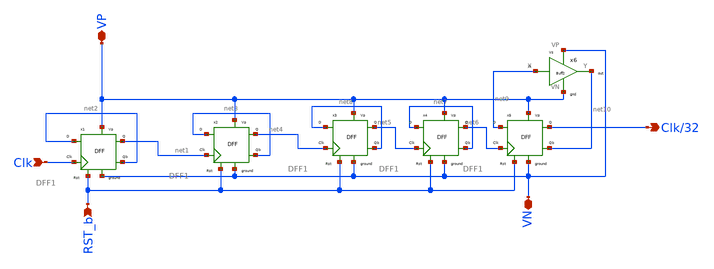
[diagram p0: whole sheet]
** sch_path: Blocks/Divide by 32 ckt/div32.sch
**.subckt div32 Clk/32 Clk VP VN RST_b
*.opin Clk/32
*.ipin Clk
*.iopin VP
*.iopin VN
*.ipin RST_b
x1 net2 Clk RST_b VN VP net1 net2 DFF1
x6 net9 net10 VN VP Buff
x2 net3 net1 RST_b VN VP net4 net3 DFF1
x3 net8 net4 RST_b VN VP net5 net8 DFF1
x4 net7 net5 RST_b VN VP net6 net7 DFF1
x5 net9 net6 RST_b VN VP Clk/32 net10 DFF1
**.ends

* expanding   symbol:  component/FlipFlops/DFF1.sym # of pins=7
** sym_path: component/FlipFlops/DFF1.sym
** sch_path: component/FlipFlops/DFF1.sch
.subckt DFF1 D Clk RST VN VP Q Qb
*.opin Q
*.iopin VN
*.iopin VP
*.ipin Clk
*.ipin D
*.ipin RST
*.opin Qb
x7 net2 net4 net3 VP VN NAND
x8 net3 Clk RST VP VN net2 NAND3
x6 Q net1 RST VP VN Qb NAND3
x4 net2 Clk net4 VP VN net1 NAND3
x5 net1 D RST VP VN net4 NAND3
x1 Qb net2 Q VP VN NAND
.ends


* expanding   symbol:  Blocks/Buffer/Buff.sym # of pins=4
** sym_path: Blocks/Buffer/Buff.sym
** sch_path: Blocks/Buffer/Buff.sch
.subckt Buff X Y VP VN
*.ipin X
*.opin Y
*.iopin VN
*.iopin VP
x1 X net1 VP VN INV
x2 net1 Y VP VN INV
.ends


* expanding   symbol:  component/NAND2/NAND.sym # of pins=5
** sym_path: component/NAND2/NAND.sym
** sch_path: component/NAND2/NAND.sch
.subckt NAND B A Y VP VN
*.iopin VP
*.ipin A
*.ipin B
*.opin Y
*.iopin VN
XM1 Y A VP VP sky130_fd_pr__pfet_01v8 L=0.15 W=1.26 nf=1 ad='int((nf+1)/2) * W/nf * 0.29' as='int((nf+2)/2) * W/nf * 0.29'
+ pd='2*int((nf+1)/2) * (W/nf + 0.29)' ps='2*int((nf+2)/2) * (W/nf + 0.29)' nrd='0.29 / W' nrs='0.29 / W'
+ sa=0 sb=0 sd=0 mult=1 m=1
XM2 Y B VP VP sky130_fd_pr__pfet_01v8 L=0.15 W=1.26 nf=1 ad='int((nf+1)/2) * W/nf * 0.29' as='int((nf+2)/2) * W/nf * 0.29'
+ pd='2*int((nf+1)/2) * (W/nf + 0.29)' ps='2*int((nf+2)/2) * (W/nf + 0.29)' nrd='0.29 / W' nrs='0.29 / W'
+ sa=0 sb=0 sd=0 mult=1 m=1
XM3 Y A net1 net1 sky130_fd_pr__nfet_01v8 L=0.15 W=0.84 nf=1 ad='int((nf+1)/2) * W/nf * 0.29' as='int((nf+2)/2) * W/nf * 0.29'
+ pd='2*int((nf+1)/2) * (W/nf + 0.29)' ps='2*int((nf+2)/2) * (W/nf + 0.29)' nrd='0.29 / W' nrs='0.29 / W'
+ sa=0 sb=0 sd=0 mult=1 m=1
XM4 net1 B VN VN sky130_fd_pr__nfet_01v8 L=0.15 W=0.84 nf=1 ad='int((nf+1)/2) * W/nf * 0.29' as='int((nf+2)/2) * W/nf * 0.29'
+ pd='2*int((nf+1)/2) * (W/nf + 0.29)' ps='2*int((nf+2)/2) * (W/nf + 0.29)' nrd='0.29 / W' nrs='0.29 / W'
+ sa=0 sb=0 sd=0 mult=1 m=1
.ends


* expanding   symbol:  component/NAND3/NAND3.sym # of pins=6
** sym_path: component/NAND3/NAND3.sym
** sch_path: component/NAND3/NAND3.sch
.subckt NAND3 A B C VP VN Y
*.iopin VP
*.iopin VN
*.ipin A
*.ipin B
*.ipin C
*.opin Y
XM1 Y A net1 VN sky130_fd_pr__nfet_01v8 L=0.15 W=1.26 nf=1 ad='int((nf+1)/2) * W/nf * 0.29' as='int((nf+2)/2) * W/nf * 0.29'
+ pd='2*int((nf+1)/2) * (W/nf + 0.29)' ps='2*int((nf+2)/2) * (W/nf + 0.29)' nrd='0.29 / W' nrs='0.29 / W'
+ sa=0 sb=0 sd=0 mult=1 m=1
XM2 net1 B net2 VN sky130_fd_pr__nfet_01v8 L=0.15 W=1.26 nf=1 ad='int((nf+1)/2) * W/nf * 0.29' as='int((nf+2)/2) * W/nf * 0.29'
+ pd='2*int((nf+1)/2) * (W/nf + 0.29)' ps='2*int((nf+2)/2) * (W/nf + 0.29)' nrd='0.29 / W' nrs='0.29 / W'
+ sa=0 sb=0 sd=0 mult=1 m=1
XM3 net2 C VN VN sky130_fd_pr__nfet_01v8 L=0.15 W=1.26 nf=1 ad='int((nf+1)/2) * W/nf * 0.29' as='int((nf+2)/2) * W/nf * 0.29'
+ pd='2*int((nf+1)/2) * (W/nf + 0.29)' ps='2*int((nf+2)/2) * (W/nf + 0.29)' nrd='0.29 / W' nrs='0.29 / W'
+ sa=0 sb=0 sd=0 mult=1 m=1
XM4 Y A VP VP sky130_fd_pr__pfet_01v8 L=0.15 W=1.26 nf=1 ad='int((nf+1)/2) * W/nf * 0.29' as='int((nf+2)/2) * W/nf * 0.29'
+ pd='2*int((nf+1)/2) * (W/nf + 0.29)' ps='2*int((nf+2)/2) * (W/nf + 0.29)' nrd='0.29 / W' nrs='0.29 / W'
+ sa=0 sb=0 sd=0 mult=1 m=1
XM5 Y B VP VP sky130_fd_pr__pfet_01v8 L=0.15 W=1.26 nf=1 ad='int((nf+1)/2) * W/nf * 0.29' as='int((nf+2)/2) * W/nf * 0.29'
+ pd='2*int((nf+1)/2) * (W/nf + 0.29)' ps='2*int((nf+2)/2) * (W/nf + 0.29)' nrd='0.29 / W' nrs='0.29 / W'
+ sa=0 sb=0 sd=0 mult=1 m=1
XM6 Y C VP VP sky130_fd_pr__pfet_01v8 L=0.15 W=1.26 nf=1 ad='int((nf+1)/2) * W/nf * 0.29' as='int((nf+2)/2) * W/nf * 0.29'
+ pd='2*int((nf+1)/2) * (W/nf + 0.29)' ps='2*int((nf+2)/2) * (W/nf + 0.29)' nrd='0.29 / W' nrs='0.29 / W'
+ sa=0 sb=0 sd=0 mult=1 m=1
.ends


* expanding   symbol:  Pico_project/INV/INV.sym # of pins=4
** sym_path: component/INV/INV.sym
** sch_path: component/INV/INV.sch
.subckt INV X Y VP VN
*.ipin X
*.opin Y
*.iopin VN
*.iopin VP
XM1 Y X VN VN sky130_fd_pr__nfet_01v8 L=0.15 W=0.42 nf=1 ad='int((nf+1)/2) * W/nf * 0.29' as='int((nf+2)/2) * W/nf * 0.29'
+ pd='2*int((nf+1)/2) * (W/nf + 0.29)' ps='2*int((nf+2)/2) * (W/nf + 0.29)' nrd='0.29 / W' nrs='0.29 / W'
+ sa=0 sb=0 sd=0 mult=1 m=1
XM2 Y X VP VP sky130_fd_pr__pfet_01v8 L=0.15 W=1.26 nf=1 ad='int((nf+1)/2) * W/nf * 0.29' as='int((nf+2)/2) * W/nf * 0.29'
+ pd='2*int((nf+1)/2) * (W/nf + 0.29)' ps='2*int((nf+2)/2) * (W/nf + 0.29)' nrd='0.29 / W' nrs='0.29 / W'
+ sa=0 sb=0 sd=0 mult=1 m=1
.ends

.end
